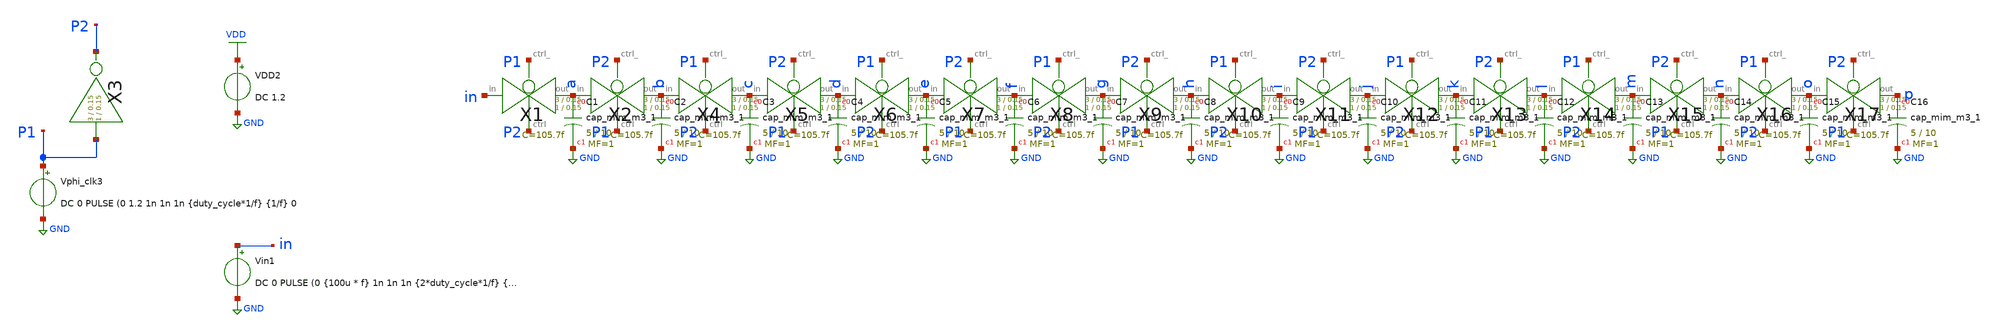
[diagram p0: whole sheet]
** sch_path: xschem/Switched_Caps/caps_multi.sch
**.subckt caps_multi
XC1 a GND sky130_fd_pr__cap_mim_m3_1 W=5 L=10 MF=1 m=1
X1 in a P1 P2 transmission_gate_set Wpmos=1 Lpmos=0.18 Wnmos=1 Lnmos=0.18
XC2 b GND sky130_fd_pr__cap_mim_m3_1 W=5 L=10 MF=1 m=1
X2 a b P2 P1 transmission_gate_set Wpmos=1 Lpmos=0.18 Wnmos=1 Lnmos=0.18
Vin1 in GND DC 0 PULSE (0 {100u * f} 1n 1n 1n {2*duty_cycle*1/f} {tend}
VDD2 VDD GND DC 1.2
Vphi_clk3 P1 GND DC 0 PULSE (0 1.2 1n 1n 1n {duty_cycle*1/f} {1/f} 0
X3 P1 P2 inv_set Wpmos=3 Lpmos=0.18 Wnmos=1 Lnmos=0.18
XC3 c GND sky130_fd_pr__cap_mim_m3_1 W=5 L=10 MF=1 m=1
X4 b c P1 P2 transmission_gate_set Wpmos=1 Lpmos=0.18 Wnmos=1 Lnmos=0.18
XC4 d GND sky130_fd_pr__cap_mim_m3_1 W=5 L=10 MF=1 m=1
X5 c d P2 P1 transmission_gate_set Wpmos=1 Lpmos=0.18 Wnmos=1 Lnmos=0.18
XC5 e GND sky130_fd_pr__cap_mim_m3_1 W=5 L=10 MF=1 m=1
X6 d e P1 P2 transmission_gate_set Wpmos=1 Lpmos=0.18 Wnmos=1 Lnmos=0.18
XC6 f GND sky130_fd_pr__cap_mim_m3_1 W=5 L=10 MF=1 m=1
X7 e f P2 P1 transmission_gate_set Wpmos=1 Lpmos=0.18 Wnmos=1 Lnmos=0.18
XC7 g GND sky130_fd_pr__cap_mim_m3_1 W=5 L=10 MF=1 m=1
X8 f g P1 P2 transmission_gate_set Wpmos=1 Lpmos=0.18 Wnmos=1 Lnmos=0.18
XC8 h GND sky130_fd_pr__cap_mim_m3_1 W=5 L=10 MF=1 m=1
X9 g h P2 P1 transmission_gate_set Wpmos=1 Lpmos=0.18 Wnmos=1 Lnmos=0.18
XC9 i GND sky130_fd_pr__cap_mim_m3_1 W=5 L=10 MF=1 m=1
X10 h i P1 P2 transmission_gate_set Wpmos=1 Lpmos=0.18 Wnmos=1 Lnmos=0.18
XC10 j GND sky130_fd_pr__cap_mim_m3_1 W=5 L=10 MF=1 m=1
X11 i j P2 P1 transmission_gate_set Wpmos=1 Lpmos=0.18 Wnmos=1 Lnmos=0.18
XC11 k GND sky130_fd_pr__cap_mim_m3_1 W=5 L=10 MF=1 m=1
X12 j k P1 P2 transmission_gate_set Wpmos=1 Lpmos=0.18 Wnmos=1 Lnmos=0.18
XC12 l GND sky130_fd_pr__cap_mim_m3_1 W=5 L=10 MF=1 m=1
X13 k l P2 P1 transmission_gate_set Wpmos=1 Lpmos=0.18 Wnmos=1 Lnmos=0.18
XC13 m GND sky130_fd_pr__cap_mim_m3_1 W=5 L=10 MF=1 m=1
X14 l m P1 P2 transmission_gate_set Wpmos=1 Lpmos=0.18 Wnmos=1 Lnmos=0.18
XC14 n GND sky130_fd_pr__cap_mim_m3_1 W=5 L=10 MF=1 m=1
X15 m n P2 P1 transmission_gate_set Wpmos=1 Lpmos=0.18 Wnmos=1 Lnmos=0.18
XC15 o GND sky130_fd_pr__cap_mim_m3_1 W=5 L=10 MF=1 m=1
X16 n o P1 P2 transmission_gate_set Wpmos=1 Lpmos=0.18 Wnmos=1 Lnmos=0.18
XC16 p GND sky130_fd_pr__cap_mim_m3_1 W=5 L=10 MF=1 m=1
X17 o p P2 P1 transmission_gate_set Wpmos=1 Lpmos=0.18 Wnmos=1 Lnmos=0.18
**** begin user architecture code


.lib /home/sky/sky130A/libs.tech/ngspice/sky130.lib.spice tt
.options abstol=1e-14 reltol=1e-4
.param f=2.56M
.param duty_cycle=0.5
.param tau={(16^2)*1/f}
.param tend={4*tau}

*start all caps with 0 charge
.ic v(a)=0 v(b)=0 v(c)=0 v(d)=0   v(e)=0 v(f)=0 v(g)=0 v(h)=0   v(i)=0 v(j)=0 v(k)=0 v(l)=0   v(m)=0
+ v(n)=0 v(o)=0 v(p)=0

*.ac DEC 100 10 20k *doesn't seem to work, get 0s out
.tran {1/f/100} {tend}
.save all


**** end user architecture code
**.ends

* expanding   symbol:  /home/sky/Desktop/fossi_cochlea/xschem/transmission_gate/transmission_gate_set.sym # of pins=4
** sym_path: xschem/transmission_gate/transmission_gate_set.sym
** sch_path: xschem/transmission_gate/transmission_gate_set.sch
.subckt transmission_gate_set in out ctrl_ ctrl  Wpmos=1 Lpmos=0.18 Wnmos=1 Lnmos=0.18
*.iopin in
*.iopin out
*.ipin ctrl_
*.ipin ctrl
XM1 in ctrl out GND sky130_fd_pr__nfet_01v8 L=0.15 W=1 nf=1 ad='int((nf+1)/2) * W/nf * 0.29' as='int((nf+2)/2)
+ * W/nf * 0.29' pd='2*int((nf+1)/2) * (W/nf + 0.29)' ps='2*int((nf+2)/2) * (W/nf + 0.29)' nrd='0.29 /
+ W' nrs='0.29 / W' sa=0 sb=0 sd=0 mult=1 m=1
XM2 out ctrl_ in VDD sky130_fd_pr__pfet_01v8 L=0.15 W=3 nf=1 ad='int((nf+1)/2) * W/nf * 0.29' as='int((nf+2)/2)
+ * W/nf * 0.29' pd='2*int((nf+1)/2) * (W/nf + 0.29)' ps='2*int((nf+2)/2) * (W/nf + 0.29)' nrd='0.29 /
+ W' nrs='0.29 / W' sa=0 sb=0 sd=0 mult=1 m=1
.ends


* expanding   symbol:  /home/sky/Desktop/fossi_cochlea/xschem/inv/inv_set.sym # of pins=2
** sym_path: xschem/inv/inv_set.sym
** sch_path: xschem/inv/inv_set.sch
.subckt inv_set in out  Wpmos=3 Lpmos=0.18 Wnmos=1 Lnmos=0.18
*.ipin in
*.iopin out
XM1 out in GND GND sky130_fd_pr__nfet_01v8 L=0.15 W=1 nf=1 ad='int((nf+1)/2) * W/nf * 0.29' as='int((nf+2)/2)
+ * W/nf * 0.29' pd='2*int((nf+1)/2) * (W/nf + 0.29)' ps='2*int((nf+2)/2) * (W/nf + 0.29)' nrd='0.29 /
+ W' nrs='0.29 / W' sa=0 sb=0 sd=0 mult=1 m=1
XM2 out in VDD VDD sky130_fd_pr__pfet_01v8 L=0.15 W=3 nf=1 ad='int((nf+1)/2) * W/nf * 0.29' as='int((nf+2)/2)
+ * W/nf * 0.29' pd='2*int((nf+1)/2) * (W/nf + 0.29)' ps='2*int((nf+2)/2) * (W/nf + 0.29)' nrd='0.29 /
+ W' nrs='0.29 / W' sa=0 sb=0 sd=0 mult=1 m=1
.ends

.GLOBAL GND
.GLOBAL VDD
.end
